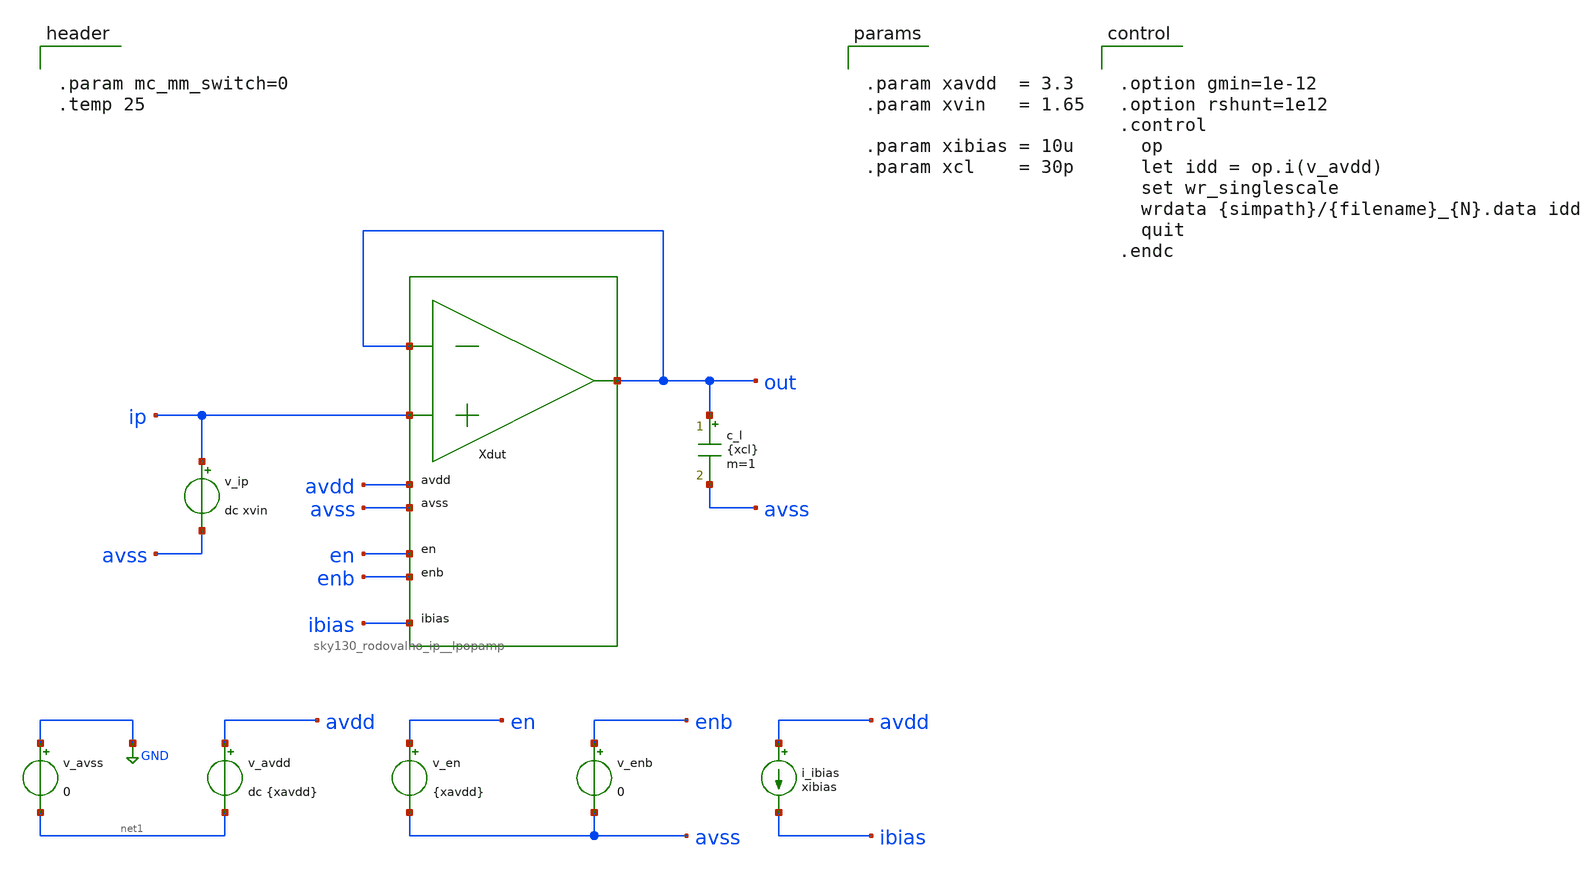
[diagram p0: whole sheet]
** sch_path: cace/tb_lpopamp_open_op.sch
**.subckt tb_lpopamp_open_op
Xdut out ip out avdd avss en enb ibias sky130_rodovalho_ip__lpopamp
v_avss GND net1 0
v_avdd avdd net1 dc {xavdd}
v_en en avss {xavdd}
v_enb enb avss 0
i_ibias avdd ibias xibias
c_l out avss {xcl} m=1
v_ip ip avss dc xvin
**** begin user architecture code


.param mc_mm_switch=0
.temp 25




.option gmin=1e-12
.option rshunt=1e12
.control
  op
  let idd = op.i(v_avdd)
  set wr_singlescale
  wrdata {simpath}/{filename}_{N}.data idd
  quit
.endc




.param xavdd  = 3.3
.param xvin   = 1.65

.param xibias = 10u
.param xcl    = 30p



** opencircuitdesign pdks install
.lib $::SKYWATER_MODELS/sky130.lib.spice tt


**** end user architecture code
**.ends
.GLOBAL GND
.end
